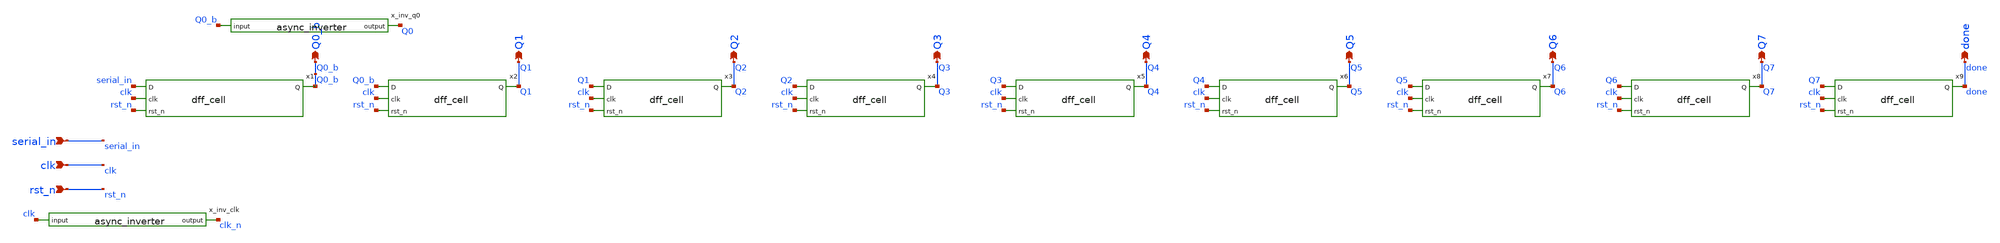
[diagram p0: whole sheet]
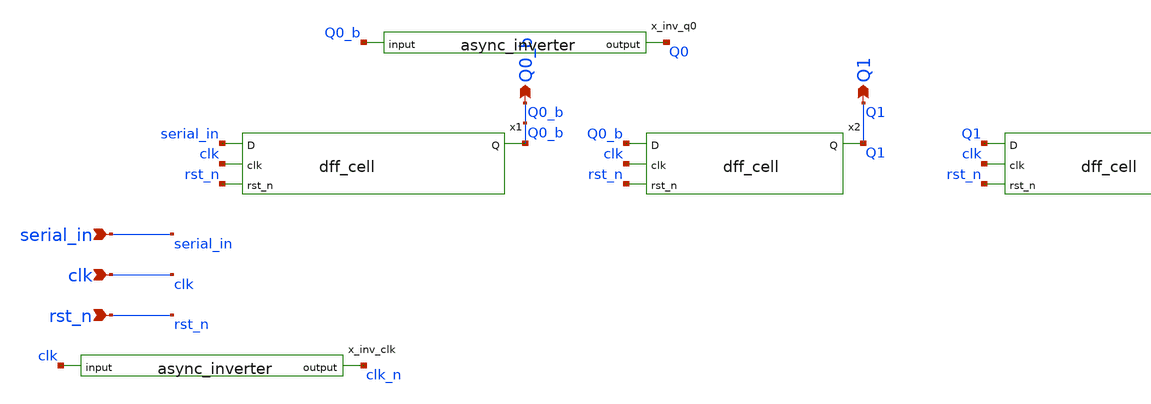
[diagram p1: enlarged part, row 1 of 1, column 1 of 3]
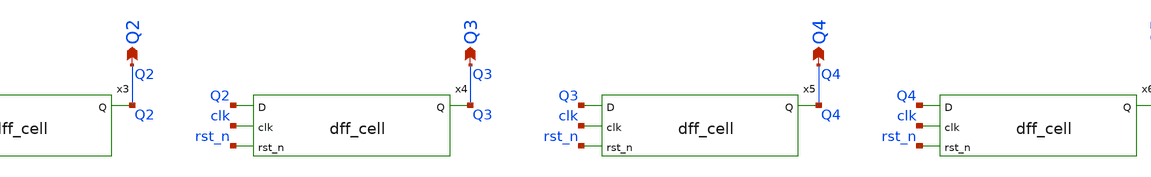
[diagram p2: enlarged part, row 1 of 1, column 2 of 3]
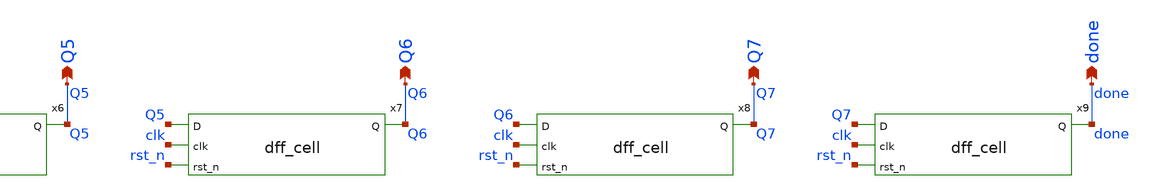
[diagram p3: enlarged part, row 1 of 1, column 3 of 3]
** sch_path: xschem/sar_adc/blocks/async_sar/shift_reg_8bit.sch
**.subckt shift_reg_8bit serial_in clk rst_n Q0_b Q1 Q2 Q3 Q4 Q5 Q6 Q7 done
*.ipin serial_in
*.ipin clk
*.ipin rst_n
*.opin Q0_b
*.opin Q1
*.opin Q2
*.opin Q3
*.opin Q4
*.opin Q5
*.opin Q6
*.opin Q7
*.opin done
x1 serial_in clk rst_n Q0_b dff_cell
x2 Q0_b clk rst_n Q1 dff_cell
x3 Q1 clk rst_n Q2 dff_cell
x4 Q2 clk rst_n Q3 dff_cell
x5 Q3 clk rst_n Q4 dff_cell
x6 Q4 clk rst_n Q5 dff_cell
x7 Q5 clk rst_n Q6 dff_cell
x8 Q6 clk rst_n Q7 dff_cell
x9 Q7 clk rst_n done dff_cell
x_inv_q0 Q0 Q0_b async_inverter
x_inv_clk clk_n clk async_inverter
**.ends

* expanding   symbol:  sar_adc/blocks/async_sar/dff_cell.sym # of pins=4
** sym_path: xschem/sar_adc/dff_cell.sym
** sch_path: xschem/sar_adc/dff_cell.sch
.subckt dff_cell D clk rst_n Q
*.ipin clk
*.ipin D
*.ipin rst_n
*.opin Q
XM1 clk_n clk VDD VDD pfet_03v3 L=0.28u W=1.0u nf=1 ad='int((nf+1)/2) * W/nf * 0.18u' as='int((nf+2)/2) * W/nf * 0.18u'
+ pd='2*int((nf+1)/2) * (W/nf + 0.18u)' ps='2*int((nf+2)/2) * (W/nf + 0.18u)' nrd='0.18u / W' nrs='0.18u / W'
+ sa=0 sb=0 sd=0 m=1
XM2 clk_n clk 0 0 nfet_03v3 L=0.28u W=0.50u nf=1 ad='int((nf+1)/2) * W/nf * 0.18u' as='int((nf+2)/2) * W/nf * 0.18u'
+ pd='2*int((nf+1)/2) * (W/nf + 0.18u)' ps='2*int((nf+2)/2) * (W/nf + 0.18u)' nrd='0.18u / W' nrs='0.18u / W'
+ sa=0 sb=0 sd=0 m=1
XM3 M clk D_int VDD pfet_03v3 L=0.28u W=1.0u nf=1 ad='int((nf+1)/2) * W/nf * 0.18u' as='int((nf+2)/2) * W/nf * 0.18u'
+ pd='2*int((nf+1)/2) * (W/nf + 0.18u)' ps='2*int((nf+2)/2) * (W/nf + 0.18u)' nrd='0.18u / W' nrs='0.18u / W'
+ sa=0 sb=0 sd=0 m=1
XM4 D_int clk_n M 0 nfet_03v3 L=0.28u W=0.50u nf=1 ad='int((nf+1)/2) * W/nf * 0.18u' as='int((nf+2)/2) * W/nf * 0.18u'
+ pd='2*int((nf+1)/2) * (W/nf + 0.18u)' ps='2*int((nf+2)/2) * (W/nf + 0.18u)' nrd='0.18u / W' nrs='0.18u / W'
+ sa=0 sb=0 sd=0 m=1
XM5 M_bar M VDD VDD pfet_03v3 L=0.28u W=1.0u nf=1 ad='int((nf+1)/2) * W/nf * 0.18u' as='int((nf+2)/2) * W/nf * 0.18u'
+ pd='2*int((nf+1)/2) * (W/nf + 0.18u)' ps='2*int((nf+2)/2) * (W/nf + 0.18u)' nrd='0.18u / W' nrs='0.18u / W'
+ sa=0 sb=0 sd=0 m=1
XM6 M_bar M 0 0 nfet_03v3 L=0.28u W=0.50u nf=1 ad='int((nf+1)/2) * W/nf * 0.18u' as='int((nf+2)/2) * W/nf * 0.18u'
+ pd='2*int((nf+1)/2) * (W/nf + 0.18u)' ps='2*int((nf+2)/2) * (W/nf + 0.18u)' nrd='0.18u / W' nrs='0.18u / W'
+ sa=0 sb=0 sd=0 m=1
XM7 M M_bar VDD VDD pfet_03v3 L=2.0u W=0.30u nf=1 ad='int((nf+1)/2) * W/nf * 0.18u' as='int((nf+2)/2) * W/nf * 0.18u'
+ pd='2*int((nf+1)/2) * (W/nf + 0.18u)' ps='2*int((nf+2)/2) * (W/nf + 0.18u)' nrd='0.18u / W' nrs='0.18u / W'
+ sa=0 sb=0 sd=0 m=1
XM8 M M_bar 0 0 nfet_03v3 L=2.4u W=0.22u nf=1 ad='int((nf+1)/2) * W/nf * 0.18u' as='int((nf+2)/2) * W/nf * 0.18u'
+ pd='2*int((nf+1)/2) * (W/nf + 0.18u)' ps='2*int((nf+2)/2) * (W/nf + 0.18u)' nrd='0.18u / W' nrs='0.18u / W'
+ sa=0 sb=0 sd=0 m=1
XM9 S clk_n M_bar VDD pfet_03v3 L=0.28u W=1.0u nf=1 ad='int((nf+1)/2) * W/nf * 0.18u' as='int((nf+2)/2) * W/nf * 0.18u'
+ pd='2*int((nf+1)/2) * (W/nf + 0.18u)' ps='2*int((nf+2)/2) * (W/nf + 0.18u)' nrd='0.18u / W' nrs='0.18u / W'
+ sa=0 sb=0 sd=0 m=1
XM10 M_bar clk S 0 nfet_03v3 L=0.28u W=0.50u nf=1 ad='int((nf+1)/2) * W/nf * 0.18u' as='int((nf+2)/2) * W/nf * 0.18u'
+ pd='2*int((nf+1)/2) * (W/nf + 0.18u)' ps='2*int((nf+2)/2) * (W/nf + 0.18u)' nrd='0.18u / W' nrs='0.18u / W'
+ sa=0 sb=0 sd=0 m=1
XM11 Q_bar S VDD VDD pfet_03v3 L=0.28u W=1.0u nf=1 ad='int((nf+1)/2) * W/nf * 0.18u' as='int((nf+2)/2) * W/nf * 0.18u'
+ pd='2*int((nf+1)/2) * (W/nf + 0.18u)' ps='2*int((nf+2)/2) * (W/nf + 0.18u)' nrd='0.18u / W' nrs='0.18u / W'
+ sa=0 sb=0 sd=0 m=1
XM12 Q_bar rst_n VDD VDD pfet_03v3 L=0.28u W=1.0u nf=1 ad='int((nf+1)/2) * W/nf * 0.18u' as='int((nf+2)/2) * W/nf * 0.18u'
+ pd='2*int((nf+1)/2) * (W/nf + 0.18u)' ps='2*int((nf+2)/2) * (W/nf + 0.18u)' nrd='0.18u / W' nrs='0.18u / W'
+ sa=0 sb=0 sd=0 m=1
XM13 Q_bar S net1 0 nfet_03v3 L=0.28u W=0.50u nf=1 ad='int((nf+1)/2) * W/nf * 0.18u' as='int((nf+2)/2) * W/nf * 0.18u'
+ pd='2*int((nf+1)/2) * (W/nf + 0.18u)' ps='2*int((nf+2)/2) * (W/nf + 0.18u)' nrd='0.18u / W' nrs='0.18u / W'
+ sa=0 sb=0 sd=0 m=1
XM14 net1 rst_n 0 0 nfet_03v3 L=0.28u W=0.50u nf=1 ad='int((nf+1)/2) * W/nf * 0.18u' as='int((nf+2)/2) * W/nf * 0.18u'
+ pd='2*int((nf+1)/2) * (W/nf + 0.18u)' ps='2*int((nf+2)/2) * (W/nf + 0.18u)' nrd='0.18u / W' nrs='0.18u / W'
+ sa=0 sb=0 sd=0 m=1
XM15 Q Q_bar VDD VDD pfet_03v3 L=0.28u W=1.0u nf=1 ad='int((nf+1)/2) * W/nf * 0.18u' as='int((nf+2)/2) * W/nf * 0.18u'
+ pd='2*int((nf+1)/2) * (W/nf + 0.18u)' ps='2*int((nf+2)/2) * (W/nf + 0.18u)' nrd='0.18u / W' nrs='0.18u / W'
+ sa=0 sb=0 sd=0 m=1
XM16 Q Q_bar 0 0 nfet_03v3 L=0.28u W=0.50u nf=1 ad='int((nf+1)/2) * W/nf * 0.18u' as='int((nf+2)/2) * W/nf * 0.18u'
+ pd='2*int((nf+1)/2) * (W/nf + 0.18u)' ps='2*int((nf+2)/2) * (W/nf + 0.18u)' nrd='0.18u / W' nrs='0.18u / W'
+ sa=0 sb=0 sd=0 m=1
XM17 S Q_bar VDD VDD pfet_03v3 L=2.0u W=0.30u nf=1 ad='int((nf+1)/2) * W/nf * 0.18u' as='int((nf+2)/2) * W/nf * 0.18u'
+ pd='2*int((nf+1)/2) * (W/nf + 0.18u)' ps='2*int((nf+2)/2) * (W/nf + 0.18u)' nrd='0.18u / W' nrs='0.18u / W'
+ sa=0 sb=0 sd=0 m=1
XM18 S Q_bar 0 0 nfet_03v3 L=2.4u W=0.22u nf=1 ad='int((nf+1)/2) * W/nf * 0.18u' as='int((nf+2)/2) * W/nf * 0.18u'
+ pd='2*int((nf+1)/2) * (W/nf + 0.18u)' ps='2*int((nf+2)/2) * (W/nf + 0.18u)' nrd='0.18u / W' nrs='0.18u / W'
+ sa=0 sb=0 sd=0 m=1
XM19 D_int D VDD VDD pfet_03v3 L=0.28u W=1.0u nf=1 ad='int((nf+1)/2) * W/nf * 0.18u' as='int((nf+2)/2) * W/nf * 0.18u'
+ pd='2*int((nf+1)/2) * (W/nf + 0.18u)' ps='2*int((nf+2)/2) * (W/nf + 0.18u)' nrd='0.18u / W' nrs='0.18u / W'
+ sa=0 sb=0 sd=0 m=1
XM20 D_int D 0 0 nfet_03v3 L=0.28u W=0.50u nf=1 ad='int((nf+1)/2) * W/nf * 0.18u' as='int((nf+2)/2) * W/nf * 0.18u'
+ pd='2*int((nf+1)/2) * (W/nf + 0.18u)' ps='2*int((nf+2)/2) * (W/nf + 0.18u)' nrd='0.18u / W' nrs='0.18u / W'
+ sa=0 sb=0 sd=0 m=1
.ends


* expanding   symbol:  sar_adc/blocks/async_sar/async_inverter.sym # of pins=2
** sym_path: xschem/sar_adc/blocks/async_sar/async_inverter.sym
** sch_path: xschem/sar_adc/blocks/async_sar/async_inverter.sch
.subckt async_inverter out input
*.ipin input
*.opin out
XM5 out input VDD VDD pfet_03v3 L=0.28u W=0.80u nf=1 ad='int((nf+1)/2) * W/nf * 0.18u' as='int((nf+2)/2) * W/nf * 0.18u'
+ pd='2*int((nf+1)/2) * (W/nf + 0.18u)' ps='2*int((nf+2)/2) * (W/nf + 0.18u)' nrd='0.18u / W' nrs='0.18u / W'
+ sa=0 sb=0 sd=0 m=1
XM6 out input 0 0 nfet_03v3 L=0.28u W=0.40u nf=1 ad='int((nf+1)/2) * W/nf * 0.18u' as='int((nf+2)/2) * W/nf * 0.18u'
+ pd='2*int((nf+1)/2) * (W/nf + 0.18u)' ps='2*int((nf+2)/2) * (W/nf + 0.18u)' nrd='0.18u / W' nrs='0.18u / W'
+ sa=0 sb=0 sd=0 m=1
.ends

.GLOBAL VDD
.end
